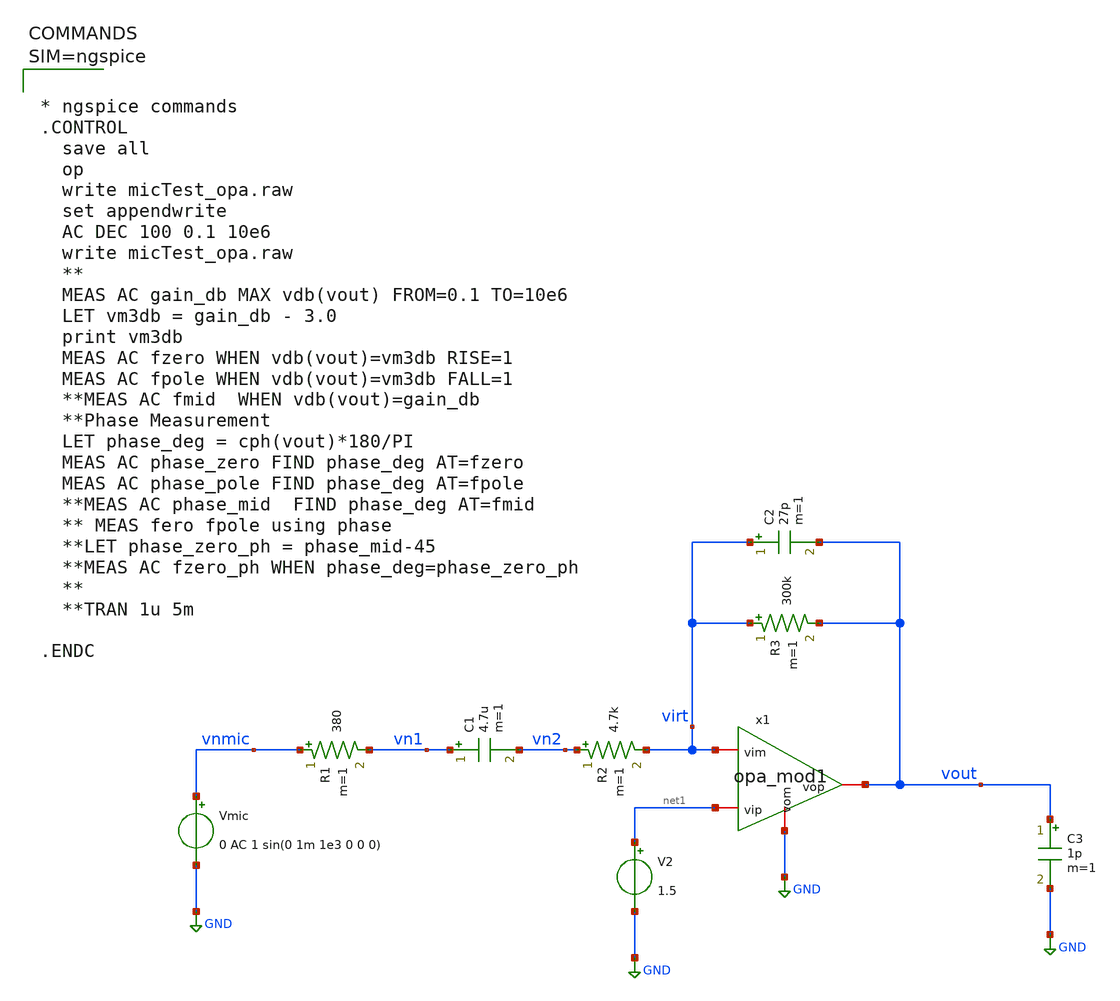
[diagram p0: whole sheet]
** sch_path: xschem/micTest_opa.sch
**.subckt micTest_opa
Vmic vnmic GND 0 AC 1 sin(0 1m 1e3 0 0 0)
R1 vnmic vn1 380 m=1
C1 vn1 vn2 4.7u m=1
R2 vn2 virt 4.7k m=1
R3 virt vout 300k m=1
C2 virt vout 27p m=1
V2 net1 GND 1.5
C3 vout GND 1p m=1
x1 vout net1 virt GND opa_mod1
**** begin user architecture code



* ngspice commands
.CONTROL
  save all
  op
  write micTest_opa.raw
  set appendwrite
  AC DEC 100 0.1 10e6
  write micTest_opa.raw
  **
  MEAS AC gain_db MAX vdb(vout) FROM=0.1 TO=10e6
  LET vm3db = gain_db - 3.0
  print vm3db
  MEAS AC fzero WHEN vdb(vout)=vm3db RISE=1
  MEAS AC fpole WHEN vdb(vout)=vm3db FALL=1
  **MEAS AC fmid  WHEN vdb(vout)=gain_db
  **Phase Measurement
  LET phase_deg = cph(vout)*180/PI
  MEAS AC phase_zero FIND phase_deg AT=fzero
  MEAS AC phase_pole FIND phase_deg AT=fpole
  **MEAS AC phase_mid  FIND phase_deg AT=fmid
  ** MEAS fero fpole using phase
  **LET phase_zero_ph = phase_mid-45
  **MEAS AC fzero_ph WHEN phase_deg=phase_zero_ph
  **
  **TRAN 1u 5m

.ENDC



**** end user architecture code
**.ends

* expanding   symbol:  opa_mod1.sym # of pins=4
** sym_path: xschem/opa_mod1.sym
** sch_path: xschem/opa_mod1.sch
.subckt opa_mod1 vop vip vim vom
*.iopin vop
*.iopin vom
*.iopin vip
*.iopin vim
E1 vilp GND vip vim 1000
R1 vilp volp 200 m=1
C1 volp GND 1u m=1
E2 vop vom volp GND 1
.ends

.GLOBAL GND
.end
